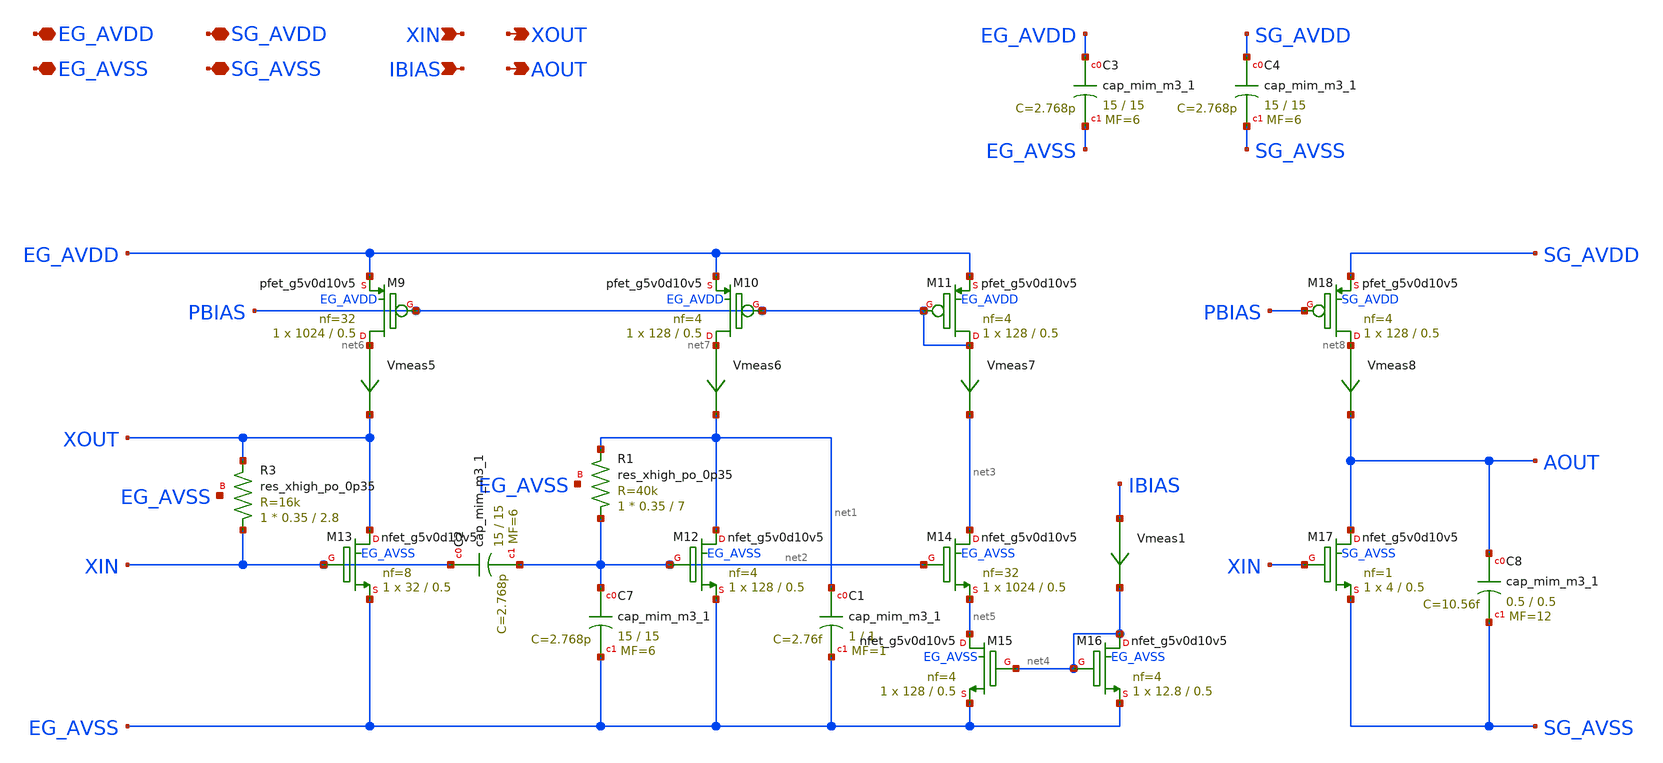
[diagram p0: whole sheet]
** sch_path: xschem/vittoz_pierce_osc.sch
**.subckt vittoz_pierce_osc EG_AVDD EG_AVSS SG_AVDD SG_AVSS XIN IBIAS XOUT AOUT
*.iopin EG_AVDD
*.iopin EG_AVSS
*.iopin SG_AVDD
*.iopin SG_AVSS
*.ipin XIN
*.ipin IBIAS
*.opin XOUT
*.opin AOUT
XM9 net6 PBIAS EG_AVDD EG_AVDD sky130_fd_pr__pfet_g5v0d10v5 L=0.5 W=1024 nf=32 ad='int((nf+1)/2) * W/nf * 0.29'
+ as='int((nf+2)/2) * W/nf * 0.29' pd='2*int((nf+1)/2) * (W/nf + 0.29)' ps='2*int((nf+2)/2) * (W/nf + 0.29)'
+ nrd='0.29 / W' nrs='0.29 / W' sa=0 sb=0 sd=0 mult=1 m=1
XM10 net7 PBIAS EG_AVDD EG_AVDD sky130_fd_pr__pfet_g5v0d10v5 L=0.5 W=128 nf=4 ad='int((nf+1)/2) * W/nf * 0.29'
+ as='int((nf+2)/2) * W/nf * 0.29' pd='2*int((nf+1)/2) * (W/nf + 0.29)' ps='2*int((nf+2)/2) * (W/nf + 0.29)'
+ nrd='0.29 / W' nrs='0.29 / W' sa=0 sb=0 sd=0 mult=1 m=1
XM11 PBIAS PBIAS EG_AVDD EG_AVDD sky130_fd_pr__pfet_g5v0d10v5 L=0.5 W=128 nf=4 ad='int((nf+1)/2) * W/nf * 0.29'
+ as='int((nf+2)/2) * W/nf * 0.29' pd='2*int((nf+1)/2) * (W/nf + 0.29)' ps='2*int((nf+2)/2) * (W/nf + 0.29)'
+ nrd='0.29 / W' nrs='0.29 / W' sa=0 sb=0 sd=0 mult=1 m=1
Vmeas5 net6 XOUT 0
.save i(vmeas5)
Vmeas6 net7 net1 0
.save i(vmeas6)
Vmeas7 PBIAS net3 0
.save i(vmeas7)
XM12 net1 net2 EG_AVSS EG_AVSS sky130_fd_pr__nfet_g5v0d10v5 L=0.5 W=128 nf=4 ad='int((nf+1)/2) * W/nf * 0.29'
+ as='int((nf+2)/2) * W/nf * 0.29' pd='2*int((nf+1)/2) * (W/nf + 0.29)' ps='2*int((nf+2)/2) * (W/nf + 0.29)'
+ nrd='0.29 / W' nrs='0.29 / W' sa=0 sb=0 sd=0 mult=1 m=1
XR1 net2 net1 EG_AVSS sky130_fd_pr__res_xhigh_po_0p35 L=7 mult=1 m=1
XC1 net1 EG_AVSS sky130_fd_pr__cap_mim_m3_1 W=1 L=1 MF=1 m=1
XC2 XIN net2 sky130_fd_pr__cap_mim_m3_1 W=15 L=15 MF=6 m=6
XC7 net2 EG_AVSS sky130_fd_pr__cap_mim_m3_1 W=15 L=15 MF=6 m=6
XM13 XOUT XIN EG_AVSS EG_AVSS sky130_fd_pr__nfet_g5v0d10v5 L=0.5 W=32 nf=8 ad='int((nf+1)/2) * W/nf * 0.29'
+ as='int((nf+2)/2) * W/nf * 0.29' pd='2*int((nf+1)/2) * (W/nf + 0.29)' ps='2*int((nf+2)/2) * (W/nf + 0.29)'
+ nrd='0.29 / W' nrs='0.29 / W' sa=0 sb=0 sd=0 mult=1 m=1
XM14 net3 net2 net5 EG_AVSS sky130_fd_pr__nfet_g5v0d10v5 L=0.5 W=1024 nf=32 ad='int((nf+1)/2) * W/nf * 0.29'
+ as='int((nf+2)/2) * W/nf * 0.29' pd='2*int((nf+1)/2) * (W/nf + 0.29)' ps='2*int((nf+2)/2) * (W/nf + 0.29)'
+ nrd='0.29 / W' nrs='0.29 / W' sa=0 sb=0 sd=0 mult=1 m=1
XM15 net5 net4 EG_AVSS EG_AVSS sky130_fd_pr__nfet_g5v0d10v5 L=0.5 W=128 nf=4 ad='int((nf+1)/2) * W/nf * 0.29'
+ as='int((nf+2)/2) * W/nf * 0.29' pd='2*int((nf+1)/2) * (W/nf + 0.29)' ps='2*int((nf+2)/2) * (W/nf + 0.29)'
+ nrd='0.29 / W' nrs='0.29 / W' sa=0 sb=0 sd=0 mult=1 m=1
XM16 net4 net4 EG_AVSS EG_AVSS sky130_fd_pr__nfet_g5v0d10v5 L=0.5 W=12.8 nf=4 ad='int((nf+1)/2) * W/nf * 0.29'
+ as='int((nf+2)/2) * W/nf * 0.29' pd='2*int((nf+1)/2) * (W/nf + 0.29)' ps='2*int((nf+2)/2) * (W/nf + 0.29)'
+ nrd='0.29 / W' nrs='0.29 / W' sa=0 sb=0 sd=0 mult=1 m=1
XR3 XIN XOUT EG_AVSS sky130_fd_pr__res_xhigh_po_0p35 L=2.8 mult=1 m=1
XM17 AOUT XIN SG_AVSS SG_AVSS sky130_fd_pr__nfet_g5v0d10v5 L=0.5 W=4 nf=1 ad='int((nf+1)/2) * W/nf * 0.29'
+ as='int((nf+2)/2) * W/nf * 0.29' pd='2*int((nf+1)/2) * (W/nf + 0.29)' ps='2*int((nf+2)/2) * (W/nf + 0.29)'
+ nrd='0.29 / W' nrs='0.29 / W' sa=0 sb=0 sd=0 mult=1 m=1
XM18 net8 PBIAS SG_AVDD SG_AVDD sky130_fd_pr__pfet_g5v0d10v5 L=0.5 W=128 nf=4 ad='int((nf+1)/2) * W/nf * 0.29'
+ as='int((nf+2)/2) * W/nf * 0.29' pd='2*int((nf+1)/2) * (W/nf + 0.29)' ps='2*int((nf+2)/2) * (W/nf + 0.29)'
+ nrd='0.29 / W' nrs='0.29 / W' sa=0 sb=0 sd=0 mult=1 m=1
Vmeas8 net8 AOUT 0
.save i(vmeas8)
XC8 AOUT SG_AVSS sky130_fd_pr__cap_mim_m3_1 W=0.5 L=0.5 MF=12 m=12
XC3 EG_AVDD EG_AVSS sky130_fd_pr__cap_mim_m3_1 W=15 L=15 MF=6 m=6
XC4 SG_AVDD SG_AVSS sky130_fd_pr__cap_mim_m3_1 W=15 L=15 MF=6 m=6
Vmeas1 IBIAS net4 0
.save i(vmeas1)
**.ends
.end
